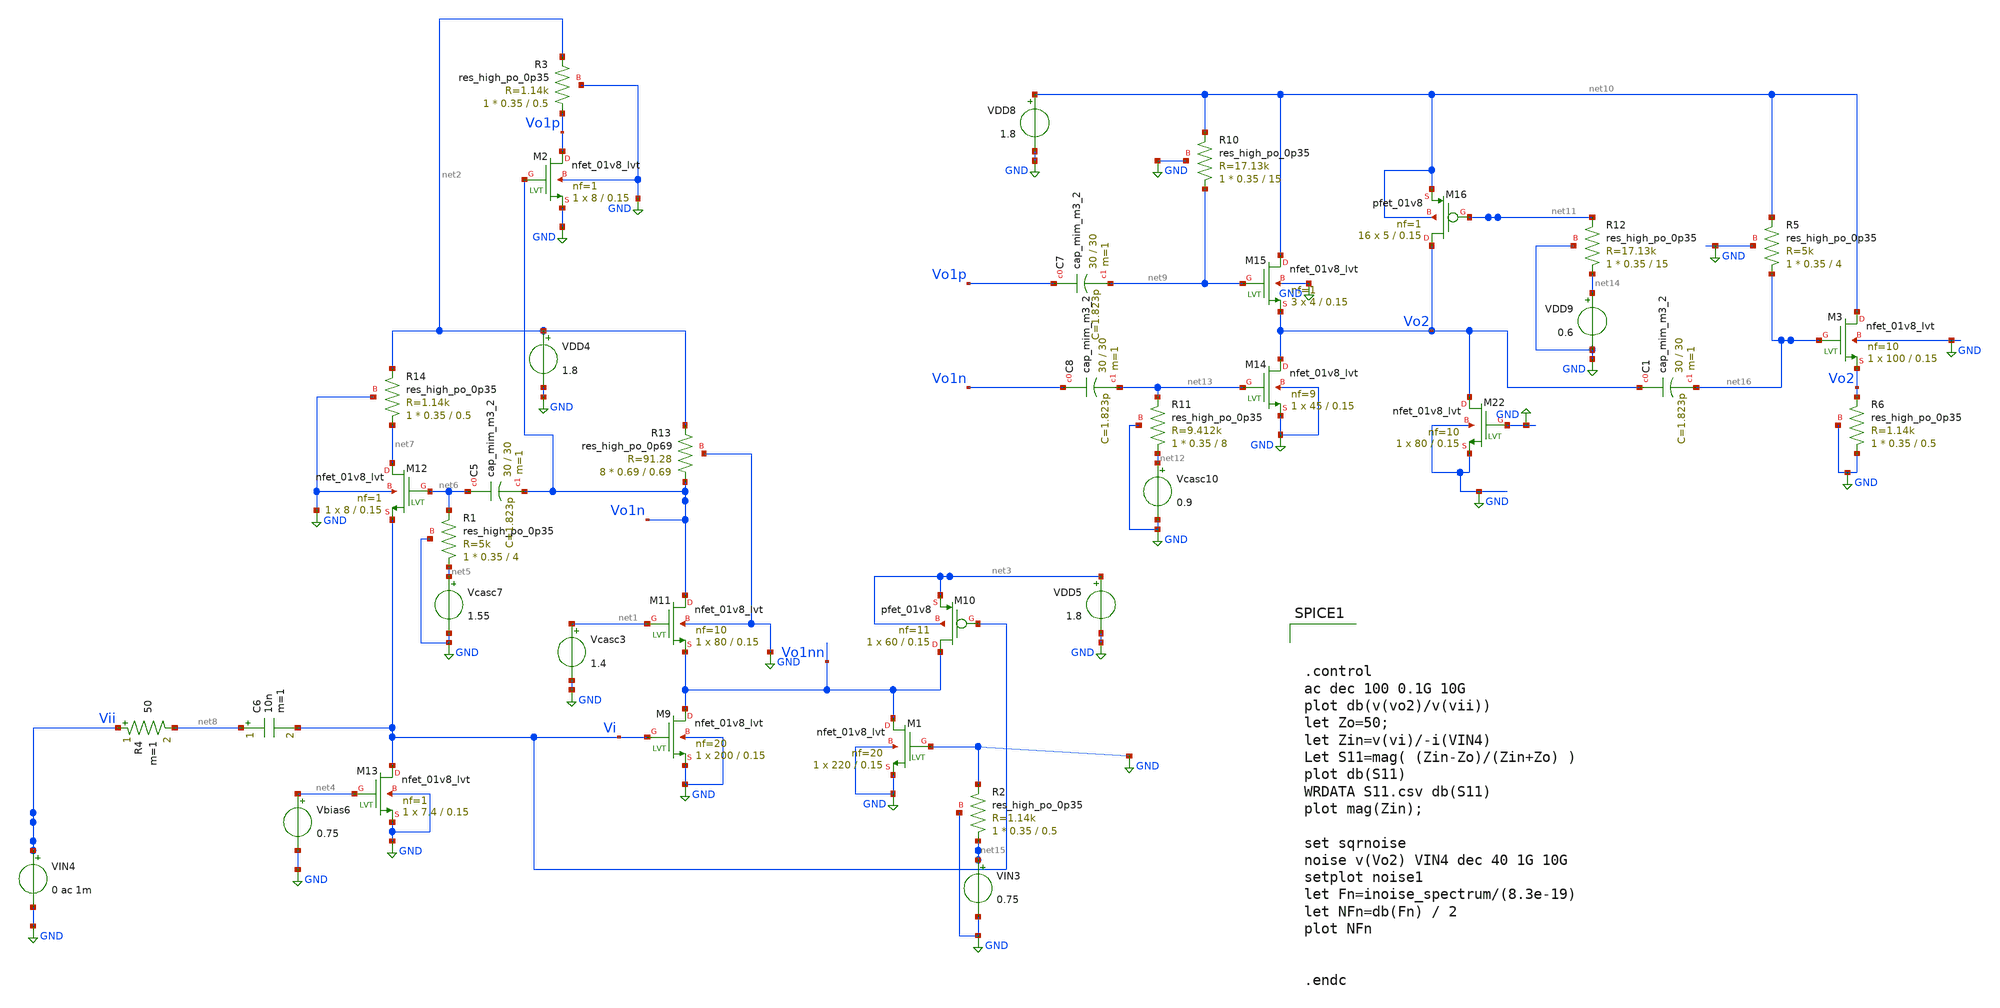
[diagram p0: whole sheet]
** sch_path: xschem/xschem4_sic_final/CompleteAMP6with50ohms1_ac.sch
**.subckt CompleteAMP6with50ohms1_ac
Vcasc3 net1 GND 1.4
VDD4 net2 GND 1.8
VDD5 net3 GND 1.8
Vbias6 net4 GND 0.75
Vcasc7 net5 GND 1.55
XR1 net5 net6 GND sky130_fd_pr__res_high_po_0p35 L=4 mult=1 m=1
XC5 net6 Vo1n sky130_fd_pr__cap_mim_m3_2 W=30 L=30 MF=1 m=1
C6 net8 Vi 10n m=1
XM9 Vo1nn Vi GND GND sky130_fd_pr__nfet_01v8_lvt L=0.15 W=200 nf=20 ad='int((nf+1)/2) * W/nf * 0.29'
+ as='int((nf+2)/2) * W/nf * 0.29' pd='2*int((nf+1)/2) * (W/nf + 0.29)' ps='2*int((nf+2)/2) * (W/nf + 0.29)'
+ nrd='0.29 / W' nrs='0.29 / W' sa=0 sb=0 sd=0 mult=1 m=1
XM10 Vo1nn Vi net3 net3 sky130_fd_pr__pfet_01v8 L=0.15 W=60 nf=11 ad='int((nf+1)/2) * W/nf * 0.29' as='int((nf+2)/2) * W/nf * 0.29'
+ pd='2*int((nf+1)/2) * (W/nf + 0.29)' ps='2*int((nf+2)/2) * (W/nf + 0.29)' nrd='0.29 / W' nrs='0.29 / W'
+ sa=0 sb=0 sd=0 mult=1 m=1
XM11 Vo1n net1 Vo1nn GND sky130_fd_pr__nfet_01v8_lvt L=0.15 W=80 nf=10 ad='int((nf+1)/2) * W/nf * 0.29'
+ as='int((nf+2)/2) * W/nf * 0.29' pd='2*int((nf+1)/2) * (W/nf + 0.29)' ps='2*int((nf+2)/2) * (W/nf + 0.29)'
+ nrd='0.29 / W' nrs='0.29 / W' sa=0 sb=0 sd=0 mult=1 m=1
XM12 net7 net6 Vi GND sky130_fd_pr__nfet_01v8_lvt L=0.15 W=8 nf=1 ad='int((nf+1)/2) * W/nf * 0.29' as='int((nf+2)/2) * W/nf * 0.29'
+ pd='2*int((nf+1)/2) * (W/nf + 0.29)' ps='2*int((nf+2)/2) * (W/nf + 0.29)' nrd='0.29 / W' nrs='0.29 / W'
+ sa=0 sb=0 sd=0 mult=1 m=1
XM13 Vi net4 GND GND sky130_fd_pr__nfet_01v8_lvt L=0.15 W=7.4 nf=1 ad='int((nf+1)/2) * W/nf * 0.29' as='int((nf+2)/2) * W/nf * 0.29'
+ pd='2*int((nf+1)/2) * (W/nf + 0.29)' ps='2*int((nf+2)/2) * (W/nf + 0.29)' nrd='0.29 / W' nrs='0.29 / W'
+ sa=0 sb=0 sd=0 mult=1 m=1
XM14 Vo2 net13 GND GND sky130_fd_pr__nfet_01v8_lvt L=0.15 W=45 nf=9 ad='int((nf+1)/2) * W/nf * 0.29'
+ as='int((nf+2)/2) * W/nf * 0.29' pd='2*int((nf+1)/2) * (W/nf + 0.29)' ps='2*int((nf+2)/2) * (W/nf + 0.29)'
+ nrd='0.29 / W' nrs='0.29 / W' sa=0 sb=0 sd=0 mult=1 m=1
XM15 net10 net9 Vo2 GND sky130_fd_pr__nfet_01v8_lvt L=0.15 W=4 nf=1 ad='int((nf+1)/2) * W/nf * 0.29'
+ as='int((nf+2)/2) * W/nf * 0.29' pd='2*int((nf+1)/2) * (W/nf + 0.29)' ps='2*int((nf+2)/2) * (W/nf + 0.29)'
+ nrd='0.29 / W' nrs='0.29 / W' sa=0 sb=0 sd=0 mult=3 m=3
XR10 net9 net10 GND sky130_fd_pr__res_high_po_0p35 L=15 mult=1 m=1
XM16 Vo2 net11 net10 net10 sky130_fd_pr__pfet_01v8 L=0.15 W=5 nf=1 ad='int((nf+1)/2) * W/nf * 0.29' as='int((nf+2)/2) * W/nf * 0.29'
+ pd='2*int((nf+1)/2) * (W/nf + 0.29)' ps='2*int((nf+2)/2) * (W/nf + 0.29)' nrd='0.29 / W' nrs='0.29 / W'
+ sa=0 sb=0 sd=0 mult=16 m=16
VDD8 net10 GND 1.8
VDD9 net14 GND 0.6
XC7 Vo1p net9 sky130_fd_pr__cap_mim_m3_2 W=30 L=30 MF=1 m=1
Vcasc10 net12 GND 0.9
XR11 net12 net13 GND sky130_fd_pr__res_high_po_0p35 L=8 mult=1 m=1
XC8 Vo1n net13 sky130_fd_pr__cap_mim_m3_2 W=30 L=30 MF=1 m=1
XR12 net14 net11 GND sky130_fd_pr__res_high_po_0p35 L=15 mult=1 m=1
XR14 net7 net2 GND sky130_fd_pr__res_high_po_0p35 L=0.5 mult=1 m=1
XM1 Vo1nn GND GND GND sky130_fd_pr__nfet_01v8_lvt L=0.15 W=220 nf=20 ad='int((nf+1)/2) * W/nf * 0.29'
+ as='int((nf+2)/2) * W/nf * 0.29' pd='2*int((nf+1)/2) * (W/nf + 0.29)' ps='2*int((nf+2)/2) * (W/nf + 0.29)'
+ nrd='0.29 / W' nrs='0.29 / W' sa=0 sb=0 sd=0 mult=1 m=1
VIN3 net15 GND 0.75
VIN4 Vii GND 0 ac 1m
XR13 Vo1n net2 GND sky130_fd_pr__res_high_po_0p69 L=0.69 mult=8 m=8
XR2 net15 GND GND sky130_fd_pr__res_high_po_0p35 L=0.5 mult=1 m=1
XM2 Vo1p Vo1n GND GND sky130_fd_pr__nfet_01v8_lvt L=0.15 W=8 nf=1 ad='int((nf+1)/2) * W/nf * 0.29' as='int((nf+2)/2) * W/nf * 0.29'
+ pd='2*int((nf+1)/2) * (W/nf + 0.29)' ps='2*int((nf+2)/2) * (W/nf + 0.29)' nrd='0.29 / W' nrs='0.29 / W'
+ sa=0 sb=0 sd=0 mult=1 m=1
XR3 Vo1p net2 GND sky130_fd_pr__res_high_po_0p35 L=0.5 mult=1 m=1
R4 Vii net8 50 m=1
XM22 Vo2 GND GND GND sky130_fd_pr__nfet_01v8_lvt L=0.15 W=80 nf=10 ad='int((nf+1)/2) * W/nf * 0.29' as='int((nf+2)/2) * W/nf * 0.29'
+ pd='2*int((nf+1)/2) * (W/nf + 0.29)' ps='2*int((nf+2)/2) * (W/nf + 0.29)' nrd='0.29 / W' nrs='0.29 / W'
+ sa=0 sb=0 sd=0 mult=1 m=1
XM3 net10 net16 Vo2 GND sky130_fd_pr__nfet_01v8_lvt L=0.15 W=100 nf=10 ad='int((nf+1)/2) * W/nf * 0.29'
+ as='int((nf+2)/2) * W/nf * 0.29' pd='2*int((nf+1)/2) * (W/nf + 0.29)' ps='2*int((nf+2)/2) * (W/nf + 0.29)'
+ nrd='0.29 / W' nrs='0.29 / W' sa=0 sb=0 sd=0 mult=1 m=1
XR5 net16 net10 GND sky130_fd_pr__res_high_po_0p35 L=4 mult=1 m=1
XC1 Vo2 net16 sky130_fd_pr__cap_mim_m3_2 W=30 L=30 MF=1 m=1
XR6 GND Vo2 GND sky130_fd_pr__res_high_po_0p35 L=0.5 mult=1 m=1
**** begin user architecture code

.lib $::SKYWATER_MODELS/sky130.lib.spice tt




.control
ac dec 100 0.1G 10G
plot db(v(vo2)/v(vii))
let Zo=50;
let Zin=v(vi)/-i(VIN4)
Let S11=mag( (Zin-Zo)/(Zin+Zo) )
plot db(S11)
WRDATA S11.csv db(S11)
plot mag(Zin);

set sqrnoise
noise v(Vo2) VIN4 dec 40 1G 10G
setplot noise1
let Fn=inoise_spectrum/(8.3e-19)
let NFn=db(Fn) / 2
plot NFn


.endc


**** end user architecture code
**.ends
.GLOBAL GND
.end
